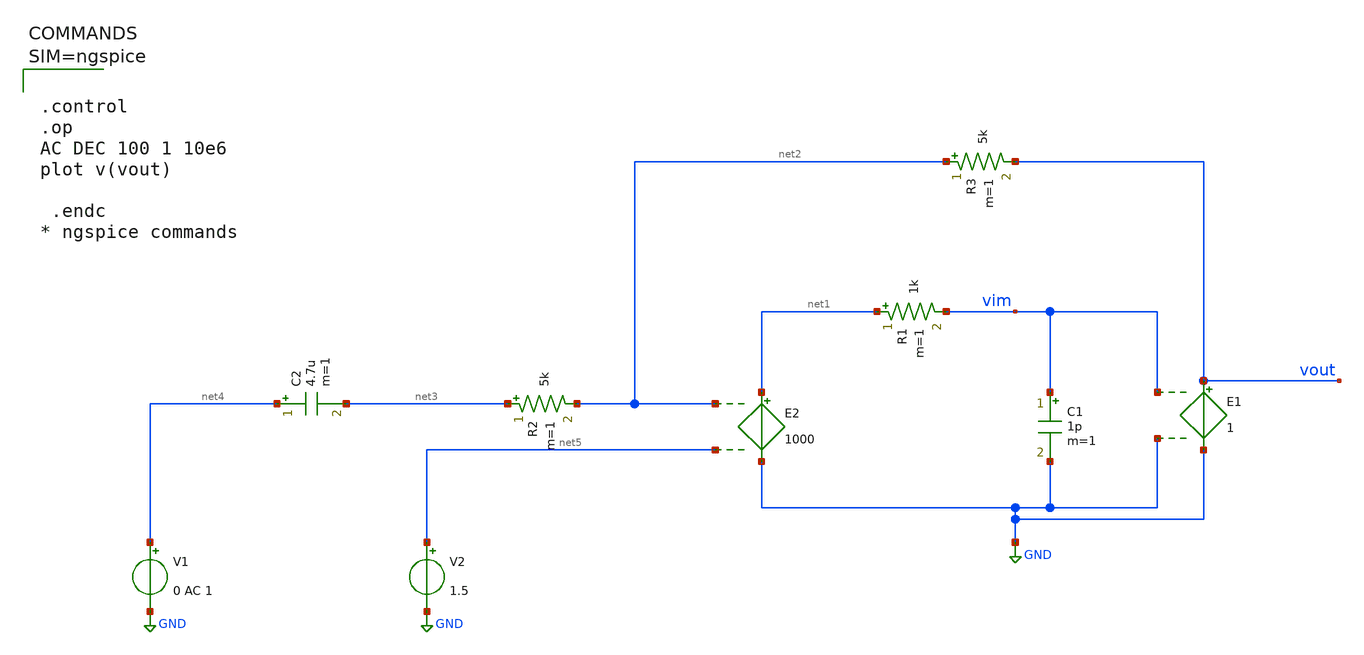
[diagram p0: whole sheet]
** sch_path: xschem/firstordermodel.sch
**.subckt firstordermodel
E1 vout GND vim GND 1
E2 net1 GND net2 net5 1000
C1 vim GND 1p m=1
R1 net1 vim 1k m=1
C2 net4 net3 4.7u m=1
R2 net3 net2 5k m=1
R3 net2 vout 5k m=1
V1 net4 GND 0 AC 1
V2 net5 GND 1.5
**** begin user architecture code



.control
.op
AC DEC 100 1 10e6
plot v(vout)

 .endc
* ngspice commands



**** end user architecture code
**.ends
.GLOBAL GND
.end
